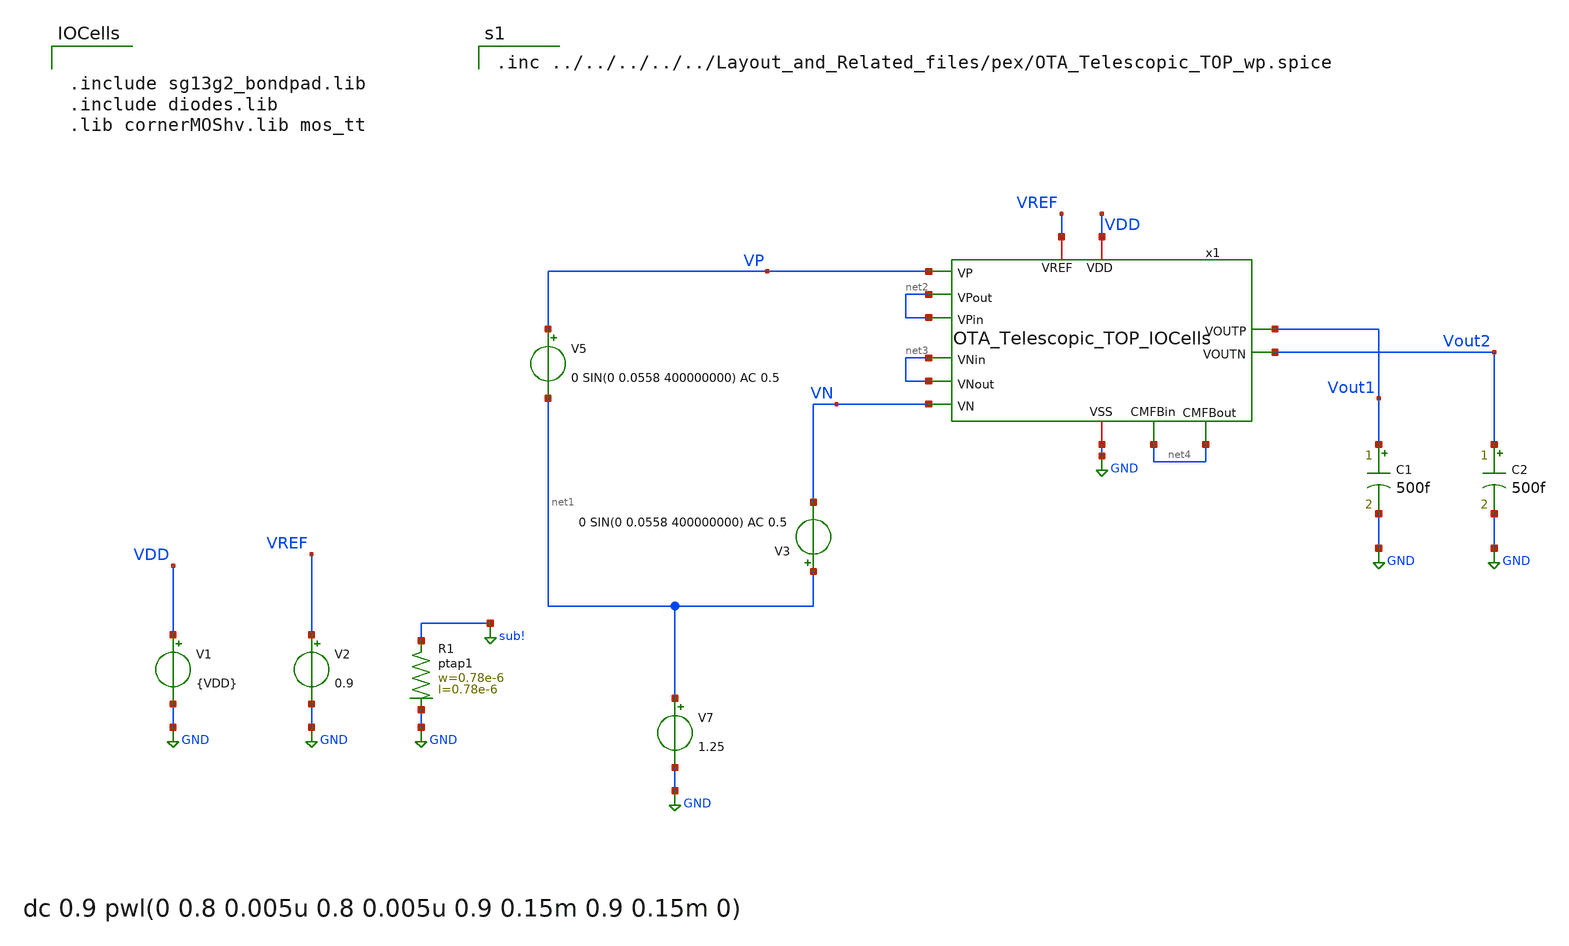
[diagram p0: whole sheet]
** sch_path: OTA_Telescopic/AutoTestbench/tb/done/OTA_Telescopic_TOP_TB_CL_TRAN400M_io.sch
**.subckt OTA_Telescopic_TOP_TB_CL_TRAN400M_io
V7 net1 GND 1.25
V5 VP net1 0 SIN(0 0.0558 400000000) AC 0.5
V1 VDD GND {VDD}
V2 VREF GND 0.9
C1 Vout1 GND 500f m=1
C2 Vout2 GND 500f m=1
V3 net1 VN 0 SIN(0 0.0558 400000000) AC 0.5
x1 VDD GND net2 VP net2 Vout2 Vout1 net3 net3 VN VREF net4 net4 OTA_Telescopic_TOP_IOCells
XR1 sub! GND ptap1 R=262.8 w=0.78e-6 l=0.78e-6
**** begin user architecture code


** opencircuitdesign pdks install
.lib cornerMOSlv.lib mos_$PROCESS
.lib cornerRES.lib res_typ
.lib cornerCAP.lib cap_typ
.temp $TEMP




.include sg13g2_bondpad.lib
.include diodes.lib
.lib cornerMOShv.lib mos_tt




.param VDD=$VDD
.nodeset v(Vout1)=0.9 v(Vout2)=0.9
.control
save VP VN Vout1 Vout2
 set color0 = white

set wr_singlescale
set wr_vecnames

save all
tran 100n 250n
*write NMOS_diode_large_signal.raw

let Vout1 = v(Vout1)
let Vout2 = v(Vout2)
let Vin = v(VP)-v(VN)

let Vout = v(Vout1)-v(Vout2)
wrdata Vout_400_io.txt Vout
wrdata Vin_400_io.txt Vin

plot Vin Vout
plot Vout1 Vout2
plot v(VP)-v(VN)
*plot v(VP) v(VN)

let Vo1 = v(x1.Vo1)
let Vo2 = v(x1.Vo2)

let Vo = Vo1-Vo2

*wrdata Vo Vo

*reset
*noise v(Vout1) V5 dec 100 1 0.5e9 1
*setplot noise1
*plot onoise_spectrum
*setplot noise2
*print onoise_total

.endc



.inc ../../../../../Layout_and_Related_files/pex/OTA_Telescopic_TOP_wp.spice

**** end user architecture code
**.ends
.GLOBAL GND
.GLOBAL sub!
.end
